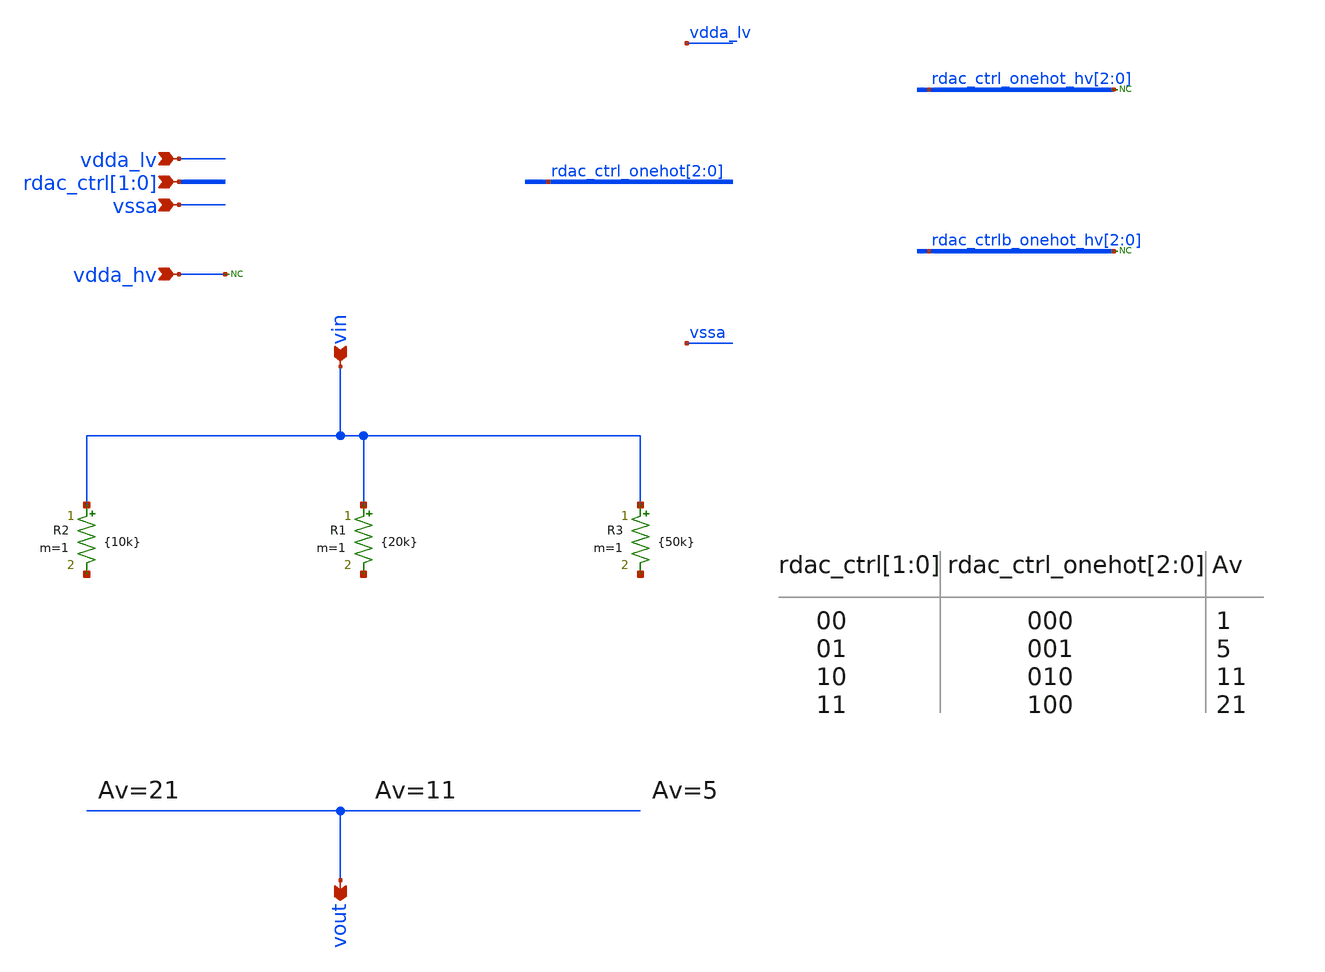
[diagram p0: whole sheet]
** sch_path: Design_Review_1/Testbench_2_tb_sunrise_ina_idealR_NOISE/rdac_no_sws_av1.sch
**.subckt rdac_no_sws_av1 vin vout vdda_lv vssa rdac_ctrl[1],rdac_ctrl[0] vdda_hv
*.ipin vin
*.opin vout
*.ipin vdda_lv
*.ipin vssa
*.ipin rdac_ctrl[1],rdac_ctrl[0]
*.ipin vdda_hv
R2 vin net1 {10k} m=1
R1 vin net2 {20k} m=1
R3 vin net3 {50k} m=1
* noconn vdda_hv
* noconn rdac_ctrl_onehot_hv[2:0]
* noconn rdac_ctrlb_onehot_hv[2:0]
**.ends
.end
